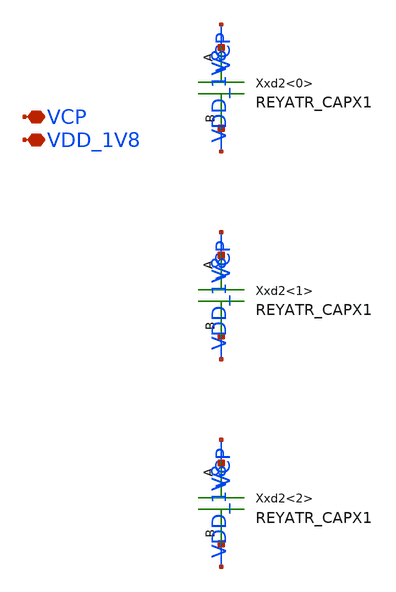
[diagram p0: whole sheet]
** sch_path: design/LELO_TEMP_SKY130A/LELOTEMP_BIAS_IBP_CAP_VCP.sch
**.subckt LELOTEMP_BIAS_IBP_CAP_VCP VCP VDD_1V8
*.iopin VCP
*.iopin VDD_1V8
Xxd2<0> VCP VDD_1V8 REYATR_CAPX1
Xxd2<1> VCP VDD_1V8 REYATR_CAPX1
Xxd2<2> VCP VDD_1V8 REYATR_CAPX1
**.ends

* expanding   symbol:  REY_ATR_SKY130A/REYATR_CAPX1.sym # of pins=2
** sym_path: design/LELO_TEMP_SKY130A/REYATR_CAPX1.sym
** sch_path: design/LELO_TEMP_SKY130A/REYATR_CAPX1.sch
.subckt REYATR_CAPX1 A B
*.iopin A
*.iopin B
XC1 B A sky130_fd_pr__cap_mim_m3_1 W=4.8 L=5 MF=1 m=1
.ends

.end
